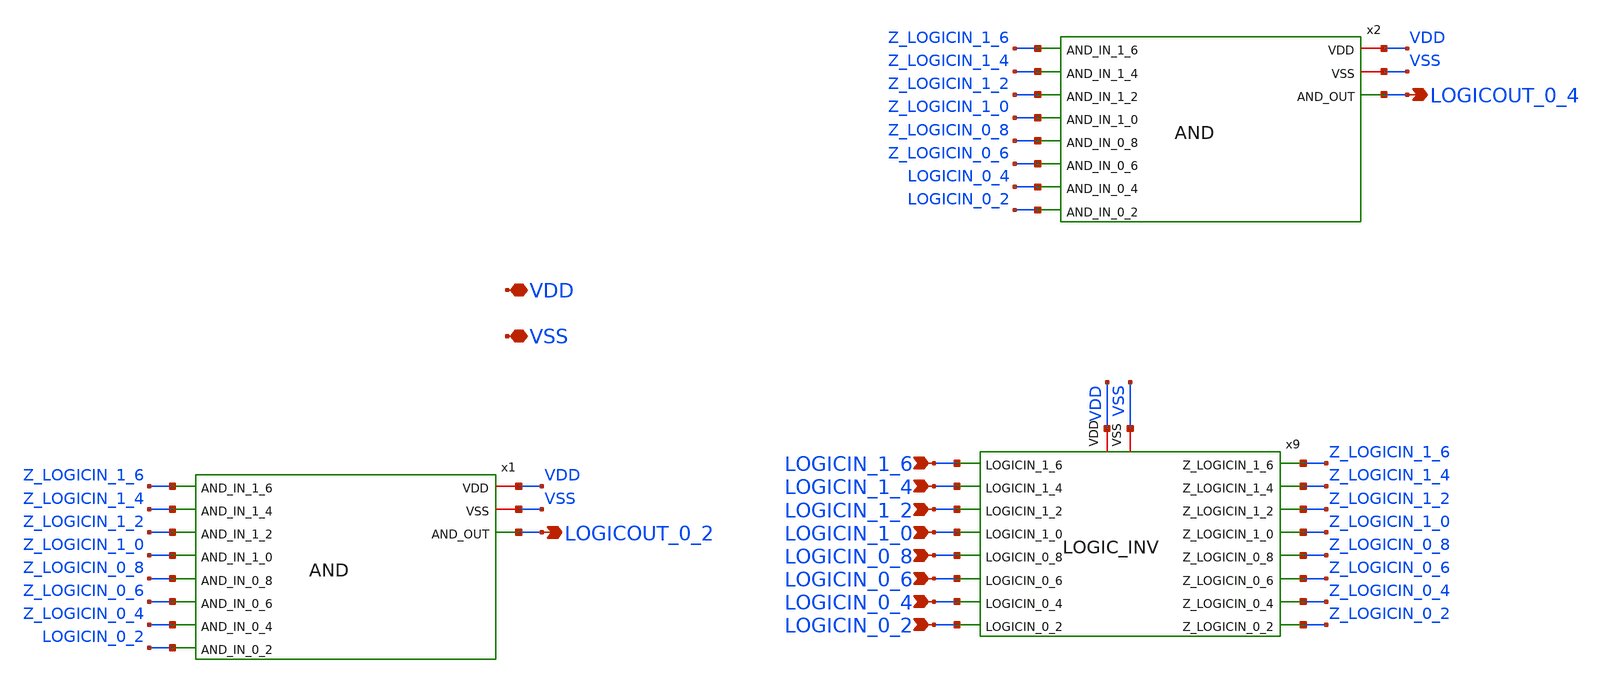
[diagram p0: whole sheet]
** sch_path: xschem/LOGIC_fix2.sch
**.subckt LOGIC_fix2 LOGICOUT_0_2 LOGICIN_1_0 LOGICIN_1_2 LOGICIN_1_4 LOGICIN_1_6 LOGICIN_0_2
*+ LOGICIN_0_4 LOGICIN_0_6 LOGICIN_0_8 VDD VSS LOGICOUT_0_4
*.opin LOGICOUT_0_2
*.ipin LOGICIN_1_0
*.ipin LOGICIN_1_2
*.ipin LOGICIN_1_4
*.ipin LOGICIN_1_6
*.ipin LOGICIN_0_2
*.ipin LOGICIN_0_4
*.ipin LOGICIN_0_6
*.ipin LOGICIN_0_8
*.iopin VDD
*.iopin VSS
*.opin LOGICOUT_0_4
x1 VDD VSS Z_LOGICIN_1_6 Z_LOGICIN_1_4 Z_LOGICIN_1_2 Z_LOGICIN_1_0 LOGICOUT_0_2 Z_LOGICIN_0_8
+ Z_LOGICIN_0_6 Z_LOGICIN_0_4 LOGICIN_0_2 AND
x9 LOGICIN_1_6 Z_LOGICIN_1_6 Z_LOGICIN_1_4 LOGICIN_1_4 LOGICIN_1_2 Z_LOGICIN_1_2 LOGICIN_1_0
+ Z_LOGICIN_1_0 Z_LOGICIN_0_8 LOGICIN_0_8 Z_LOGICIN_0_6 LOGICIN_0_6 LOGICIN_0_4 Z_LOGICIN_0_4 LOGICIN_0_2
+ Z_LOGICIN_0_2 VDD VSS LOGIC_INV
x2 VDD VSS Z_LOGICIN_1_6 Z_LOGICIN_1_4 Z_LOGICIN_1_2 Z_LOGICIN_1_0 LOGICOUT_0_4 Z_LOGICIN_0_8
+ Z_LOGICIN_0_6 LOGICIN_0_4 LOGICIN_0_2 AND
**.ends
.end
